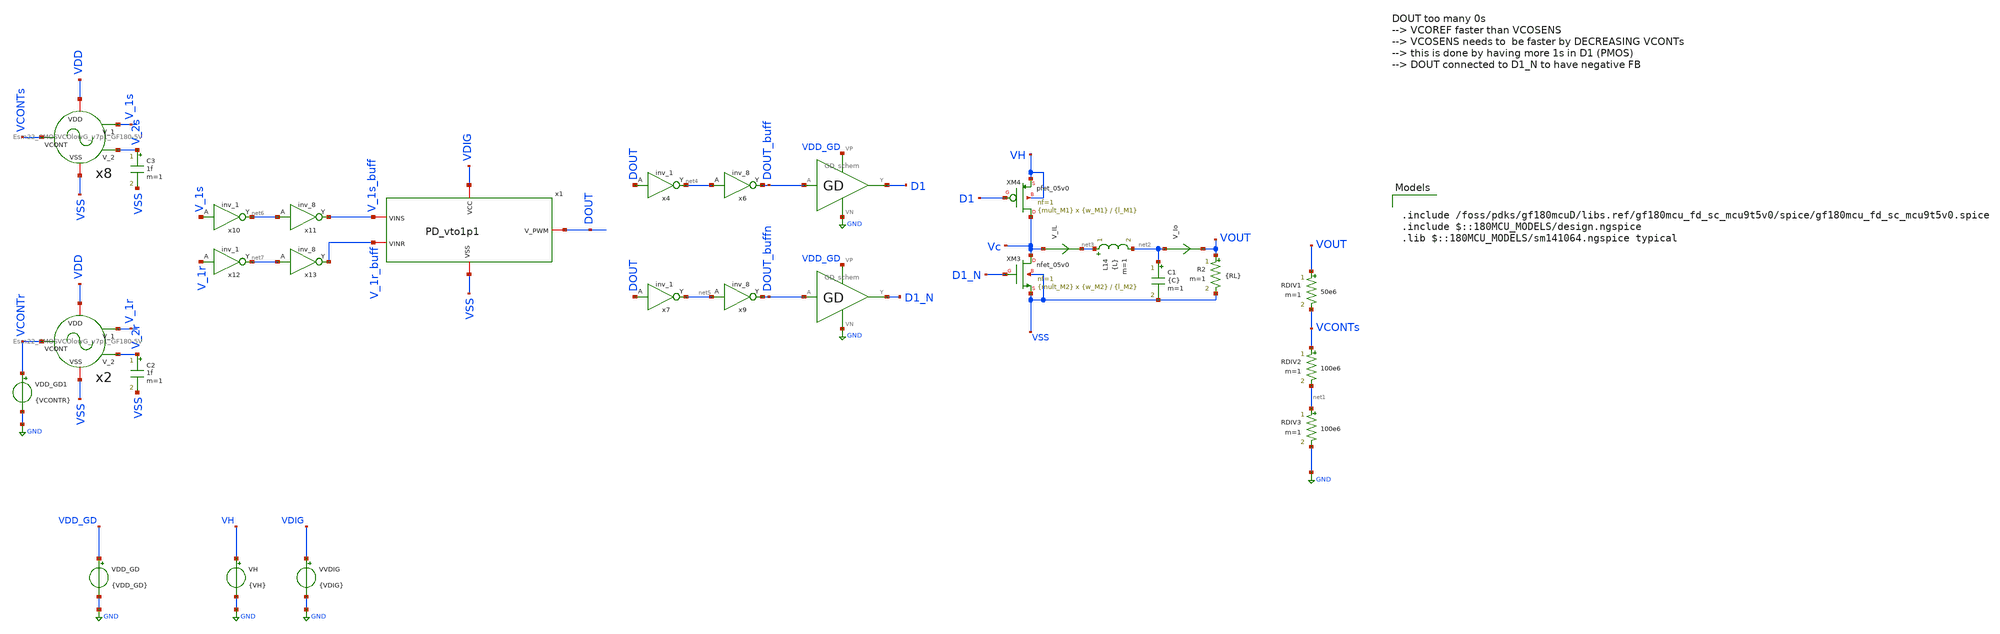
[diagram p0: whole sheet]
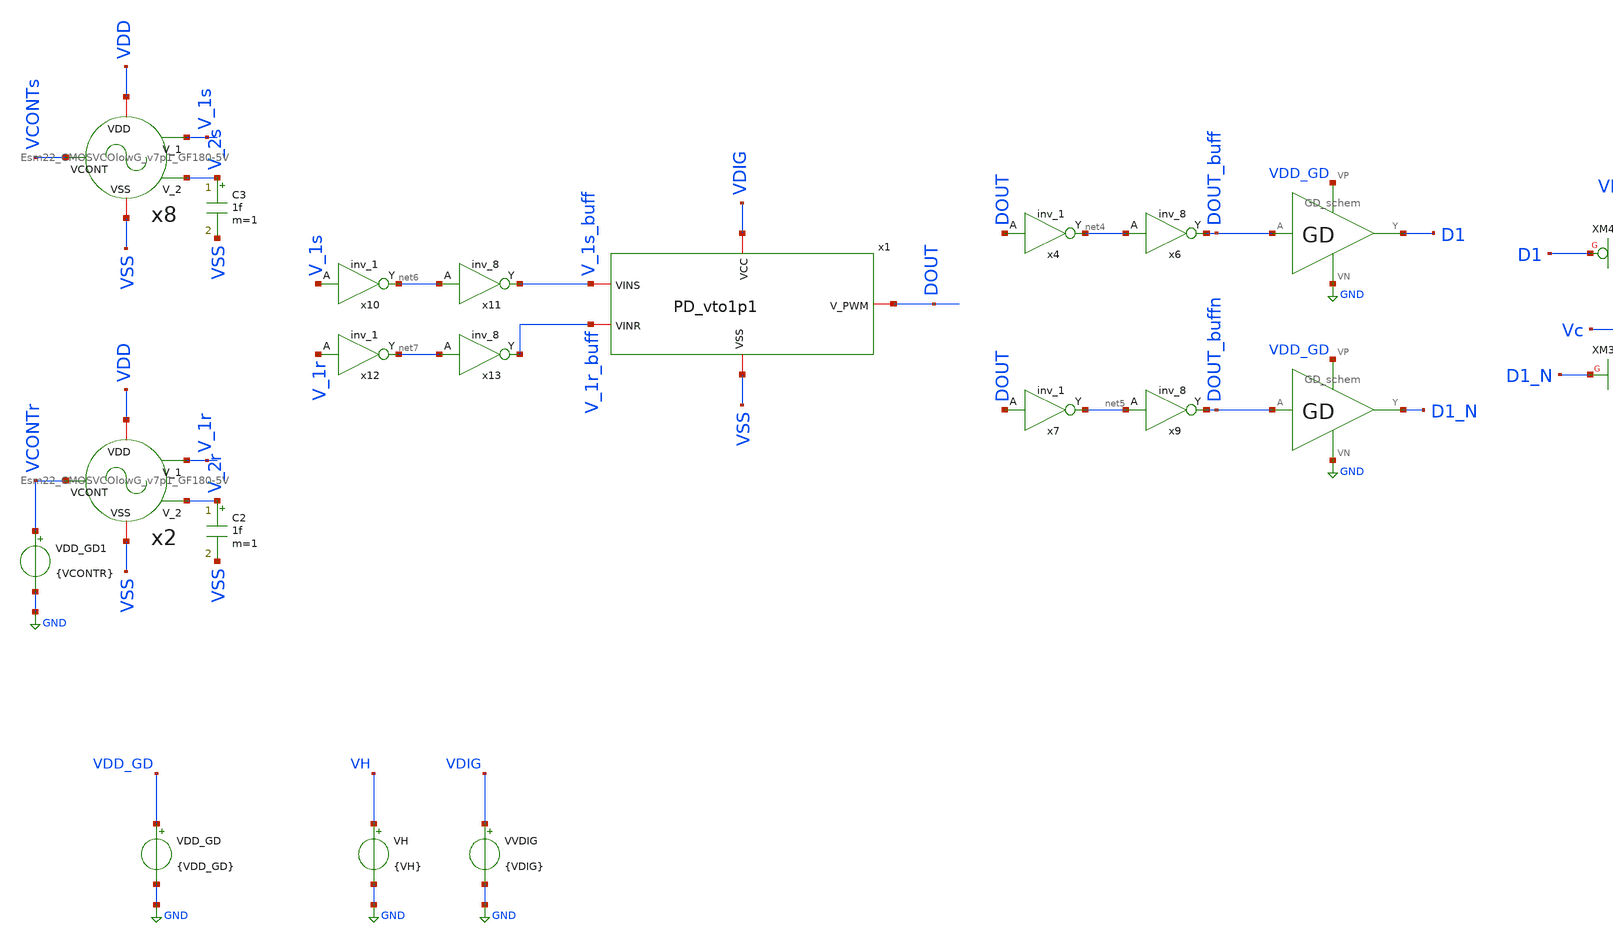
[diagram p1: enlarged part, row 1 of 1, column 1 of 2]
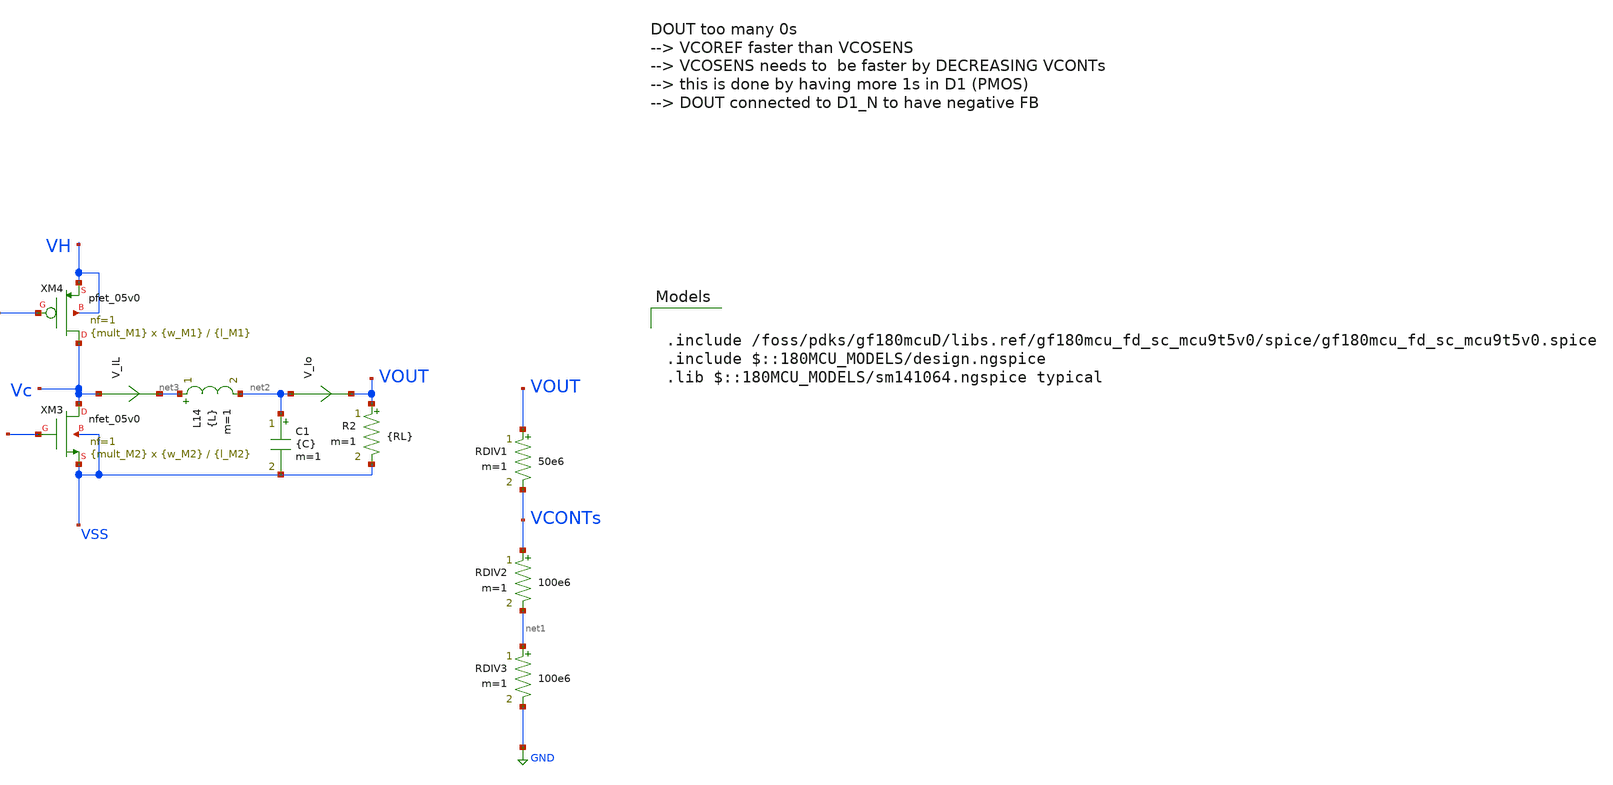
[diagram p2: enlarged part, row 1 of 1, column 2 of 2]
** sch_path: xschem/top/tb_TDBuckTOP-IHP-CL_v7p1.sch
**.subckt tb_TDBuckTOP-IHP-CL_v7p1
VH VH GND {VH}
VVDIG VDIG GND {VDIG}
RDIV1 VOUT VCONTs 50e6 m=1
RDIV2 VCONTs net1 100e6 m=1
RDIV3 net1 GND 100e6 m=1
VDD_GD VDD_GD GND {VDD_GD}
L14 net3 net2 {L} m=1
C1 net2 VSS {C} m=1
V_Io net2 VOUT 0
.save i(v_io)
V_IL Vc net3 0
.save i(v_il)
R2 VOUT VSS {RL} m=1
XM3 Vc D1_N VSS VSS nfet_05v0 L={l_M2} W={w_M2} nf=1 ad='int((nf+1)/2) * W/nf * 0.18u' as='int((nf+2)/2) * W/nf * 0.18u'
+ pd='2*int((nf+1)/2) * (W/nf + 0.18u)' ps='2*int((nf+2)/2) * (W/nf + 0.18u)' nrd='0.18u / W' nrs='0.18u / W'
+ sa=0 sb=0 sd=0 m={mult_M2}
XM4 Vc D1 VH VH pfet_05v0 L={l_M1} W={w_M1} nf=1 ad='int((nf+1)/2) * W/nf * 0.18u' as='int((nf+2)/2) * W/nf * 0.18u'
+ pd='2*int((nf+1)/2) * (W/nf + 0.18u)' ps='2*int((nf+2)/2) * (W/nf + 0.18u)' nrd='0.18u / W' nrs='0.18u / W'
+ sa=0 sb=0 sd=0 m={mult_M1}
x1 VDIG VSS V_1s_buff DOUT V_1r_buff PD_vto1p1
x8 VCONTs VSS VDD V_1s V_2s Esm22_CMOSVCOlowG_v7p1_GF180-5V
x2 VCONTr VSS VDD V_1r V_2r Esm22_CMOSVCOlowG_v7p1_GF180-5V
C2 V_2r VSS 1f m=1
C3 V_2s VSS 1f m=1
X3 VDD_GD GND DOUT_buff D1 GD_schem
X5 VDD_GD GND DOUT_buffn D1_N GD_schem
x4 DOUT VSS VDIG VSS VDIG net4 gf180mcu_fd_sc_mcu9t5v0__inv_1
x6 net4 VSS VDIG VSS VDIG DOUT_buff gf180mcu_fd_sc_mcu9t5v0__inv_8
x7 DOUT VSS VDIG VSS VDIG net5 gf180mcu_fd_sc_mcu9t5v0__inv_1
x9 net5 VSS VDIG VSS VDIG DOUT_buffn gf180mcu_fd_sc_mcu9t5v0__inv_8
VDD_GD1 VCONTr GND {VCONTR}
x10 V_1s VSS VDIG VSS VDIG net6 gf180mcu_fd_sc_mcu9t5v0__inv_1
x11 net6 VSS VDIG VSS VDIG V_1s_buff gf180mcu_fd_sc_mcu9t5v0__inv_8
x12 V_1r VSS VDIG VSS VDIG net7 gf180mcu_fd_sc_mcu9t5v0__inv_1
x13 net7 VSS VDIG VSS VDIG V_1r_buff gf180mcu_fd_sc_mcu9t5v0__inv_8
**** begin user architecture code

.param VDIG = 5
.param VH = 5
.param VDD_GD = 5
.param VCONTR = 2.64
*LATEST TDBuckLOADS
*300mA
.param RL = 6
*270mA
*.param RL = 6.67
*240mA
*.param RL = 7.5
*210mA
*.param RL = 8.57
*180mA
*.param RL = 10
*150mA
*.param RL = 12
*120mA
*.param RL = 15
*60mA
*.param RL = 30
*30mA
*.param RL = 60
*15mA
*.param RL = 120
.save v(VOUT) v(D1) v(D1_N) v(DOUT) v(VCONTr) v(VCONTs) v(V_1r) v(V_1s) v(DOUT_buff) v(DOUT_buffn) v(vh) i(vh) v(vdd_gd) i(vdd_gd) i(v_res) v(VCONTs_OL) v(vcp) v(vcn) i(vldo_out) i(vvdig) i(vvdd)
*.save all
vvdd vdd 0 dc 5
vvss vss 0 0
*vvconts VCONTs 0 dc 0.61
*.option temp = 200
.ic v(VCONTs) = 2
.ic v(V_1s) = 2
.ic v(V_2s) = 4
.ic v(V_1r) = 5
.ic v(V_2r) = 0
.ic v(VOUT) = 2.5

.control
*tran 2n 1m
*tran 4n 250u
tran 100p 30u
*wrdata /foss/designs/TO202406_CMOSVCO_Esm22/xschem/data/dataVSENS_2xCMOSVCOnDFF_v1p1.txt v(V_1s)
*+ tran1.v(V_1s) tran2.v(V_1s) tran3.v(V_1s) tran4.v(V_1s) tran5.v(V_1s) tran6.v(V_1s) tran7.v(V_1s) tran8.v(V_1s)
*+ tran9.v(V_1s) tran10.v(V_1s) tran11.v(V_1s) tran12.v(V_1s) tran13.v(V_1s) tran14.v(V_1s) tran15.v(V_1s)
*+ tran16.v(V_1s) tran17.v(V_1s) tran18.v(V_1s) tran19.v(V_1s)
*wrdata /foss/designs/TO202406_CMOSVCO_Esm22/xschem/data/data_TDBuckTOP-CL_v5p3_RL60.txt tran.v(vh)
*+ tran.i(vh) tran.v(VOUT) tran.i(vldo_out) tran.v(vh_gd) tran.i(vh_gd) tran.i(vvdig) tran.i(vvdd)
plot v(VOUT)
plot v(v_res)
plot v(D1) v(D1_N)+5
plot v(DOUT)
plot v(V_1s)+5 v(V_1r)+10
plot v(VCONTr) v(VCONTs)
*plot v(VCONTs_OL)
.endc





*PMOS
.param mult_gd_p = 72
.param w_gd_p = 6.4u
.param l_gd_p = 0.5u
*NMOS
.param mult_gd_n = 72
.param w_gd_n = 2u
.param l_gd_n = 0.6u





.param temp=27
.param mult_M1 = 2000
.param w_M1 =10u
.param l_M1 = 0.5u


.param mult_M2 = 625
.param w_M2 =10u
.param l_M2 =0.6u

*PMOS
.param mult_gd_p = 72
.param w_gd_p = 6.4u
.param l_gd_p = 0.5u
*NMOS
.param mult_gd_n = 72
.param w_gd_n = 2u
.param l_gd_n = 0.6u






*.param L = 550n
*.param R = 16.7
*.param C = 640n
.param L = 220n
*.param L = 440n
*.param C = 1u
.param C = 150n
*.param C = 300n




.include /foss/pdks/gf180mcuD/libs.ref/gf180mcu_fd_sc_mcu9t5v0/spice/gf180mcu_fd_sc_mcu9t5v0.spice
.include $::180MCU_MODELS/design.ngspice
.lib $::180MCU_MODELS/sm141064.ngspice typical

**** end user architecture code
**.ends

* expanding   symbol:  gf180_digital/PD/PD_vto1p1.sym # of pins=5
** sym_path: xschem/gf180_digital/PD/PD_vto1p1.sym
** sch_path: xschem/gf180_digital/PD/PD_vto1p1.sch
.subckt PD_vto1p1 VCC VSS VINS V_PWM VINR
*.iopin V_PWM
*.iopin VCC
*.iopin VSS
*.iopin VINS
*.iopin VINR
C2 VFE1 VSS 100f m=1
C1 VFE1 VSS 100f m=1
x1 V_N net1 VSS VCC VSS VCC V_PWM gf180mcu_fd_sc_mcu9t5v0__nor2_1
x3 VCC VSS VFE1 VINR net2 SPG_vto1p1
x2 VCC VSS VFE1 VINS net1 SPG_vto1p1
x4 net2 V_PWM VSS VCC VSS VCC V_N gf180mcu_fd_sc_mcu9t5v0__nor2_1
.ends


* expanding   symbol:  vco/Esm22_CMOSVCOlowG_v7p1_GF180-5V.sym # of pins=5
** sym_path: xschem/vco/Esm22_CMOSVCOlowG_v7p1_GF180-5V.sym
** sch_path: xschem/vco/Esm22_CMOSVCOlowG_v7p1_GF180-5V.sch
.subckt Esm22_CMOSVCOlowG_v7p1_GF180-5V VCONT VSS VDD V_1 V_2
*.ipin VCONT
*.iopin VDD
*.iopin VSS
*.opin V_1
*.opin V_2
x1 VDD VCONT V_1 V_5 VSS stage_v7p1_GF180-5V
x2 VDD VCONT V_2 V_1 VSS stage_v7p1_GF180-5V
x3 VDD VCONT V_3 V_2 VSS stage_v7p1_GF180-5V
x4 VDD VCONT V_4 V_3 VSS stage_v7p1_GF180-5V
x5 VDD VCONT V_5 V_4 VSS stage_v7p1_GF180-5V
.ends


* expanding   symbol:  pwr_stage/GD_schem.sym # of pins=4
** sym_path: pwr_stage/GD_schem.sym
** sch_path: pwr_stage/GD_schem.sch
.subckt GD_schem VP VN A Y
*.ipin A
*.iopin VP
*.iopin VN
*.opin Y
XM11 Y net1 VN VN nfet_05v0 L={l_gd_n} W={w_gd_n} nf=1 ad='int((nf+1)/2) * W/nf * 0.18u' as='int((nf+2)/2) * W/nf * 0.18u'
+ pd='2*int((nf+1)/2) * (W/nf + 0.18u)' ps='2*int((nf+2)/2) * (W/nf + 0.18u)' nrd='0.18u / W' nrs='0.18u / W'
+ sa=0 sb=0 sd=0 m={mult_gd_n}
XM12 Y net1 VP VP pfet_05v0 L={l_gd_p} W={w_gd_p} nf=1 ad='int((nf+1)/2) * W/nf * 0.18u' as='int((nf+2)/2) * W/nf * 0.18u'
+ pd='2*int((nf+1)/2) * (W/nf + 0.18u)' ps='2*int((nf+2)/2) * (W/nf + 0.18u)' nrd='0.18u / W' nrs='0.18u / W'
+ sa=0 sb=0 sd=0 m={mult_gd_p}
XM13 net1 A VN VN nfet_05v0 L={l_gd_n} W={w_gd_n} nf=1 ad='int((nf+1)/2) * W/nf * 0.18u' as='int((nf+2)/2) * W/nf * 0.18u'
+ pd='2*int((nf+1)/2) * (W/nf + 0.18u)' ps='2*int((nf+2)/2) * (W/nf + 0.18u)' nrd='0.18u / W' nrs='0.18u / W'
+ sa=0 sb=0 sd=0 m={mult_gd_n}/4
XM14 net1 A VP VP pfet_05v0 L={l_gd_p} W={w_gd_p} nf=1 ad='int((nf+1)/2) * W/nf * 0.18u' as='int((nf+2)/2) * W/nf * 0.18u'
+ pd='2*int((nf+1)/2) * (W/nf + 0.18u)' ps='2*int((nf+2)/2) * (W/nf + 0.18u)' nrd='0.18u / W' nrs='0.18u / W'
+ sa=0 sb=0 sd=0 m={mult_gd_p}/4
.ends


* expanding   symbol:  gf180_digital/SPG/SPG_vto1p1.sym # of pins=5
** sym_path: xschem/gf180_digital/SPG/SPG_vto1p1.sym
** sch_path: xschem/gf180_digital/SPG/SPG_vto1p1.sch
.subckt SPG_vto1p1 VDDd VSSd VFE VIN VRE
*.iopin VIN
*.iopin VFE
*.iopin VRE
*.iopin VDDd
*.iopin VSSd
x2 predly VSSd VDDd VSSd VDDd net2 gf180mcu_fd_sc_mcu9t5v0__inv_1
x3 vinn VSSd VDDd VSSd VDDd predly gf180mcu_fd_sc_mcu9t5v0__inv_1
x4 dly8 VSSd VDDd VSSd VDDd net1 gf180mcu_fd_sc_mcu9t5v0__inv_1
x5 VIN VSSd VDDd VSSd VDDd vinn gf180mcu_fd_sc_mcu9t5v0__inv_2
x6 predly VSSd VDDd VSSd VDDd V_gatein gf180mcu_fd_sc_mcu9t5v0__inv_8
x9 VDDd VSSd V_gatein dly7 large_delay_vto1p1
x1 dly7 VSSd VDDd VSSd VDDd dly8 gf180mcu_fd_sc_mcu9t5v0__inv_8
x8 net2 dly8 VFE VDDd VDDd VSSd VSSd gf180mcu_fd_sc_mcu9t5v0__and2_1
x7 net1 predly VRE VDDd VDDd VSSd VSSd gf180mcu_fd_sc_mcu9t5v0__and2_1
.ends


* expanding   symbol:  vco/stage_v7p1_GF180-5V.sym # of pins=5
** sym_path: xschem/vco/stage_v7p1_GF180-5V.sym
** sch_path: xschem/vco/stage_v7p1_GF180-5V.sch
.subckt stage_v7p1_GF180-5V VDD VCONT VOUT VIN VSS
*.ipin VIN
*.opin VOUT
*.iopin VDD
*.iopin VSS
*.ipin VCONT
XMN1 net4 net4 VSS VSS nfet_05v0 L=0.70u W=7u nf=7 ad='int((nf+1)/2) * W/nf * 0.18u' as='int((nf+2)/2) * W/nf * 0.18u'
+ pd='2*int((nf+1)/2) * (W/nf + 0.18u)' ps='2*int((nf+2)/2) * (W/nf + 0.18u)' nrd='0.18u / W' nrs='0.18u / W'
+ sa=0 sb=0 sd=0 m=1
XMN2 net3 net4 VSS VSS nfet_05v0 L=0.70u W=7u nf=7 ad='int((nf+1)/2) * W/nf * 0.18u' as='int((nf+2)/2) * W/nf * 0.18u'
+ pd='2*int((nf+1)/2) * (W/nf + 0.18u)' ps='2*int((nf+2)/2) * (W/nf + 0.18u)' nrd='0.18u / W' nrs='0.18u / W'
+ sa=0 sb=0 sd=0 m=1
XMN3 net2 net4 VSS VSS nfet_05v0 L=0.70u W=4u nf=4 ad='int((nf+1)/2) * W/nf * 0.18u' as='int((nf+2)/2) * W/nf * 0.18u'
+ pd='2*int((nf+1)/2) * (W/nf + 0.18u)' ps='2*int((nf+2)/2) * (W/nf + 0.18u)' nrd='0.18u / W' nrs='0.18u / W'
+ sa=0 sb=0 sd=0 m=1
XMN4 VOUT VIN net2 VSS nfet_05v0 L=5u W=2u nf=1 ad='int((nf+1)/2) * W/nf * 0.18u' as='int((nf+2)/2) * W/nf * 0.18u'
+ pd='2*int((nf+1)/2) * (W/nf + 0.18u)' ps='2*int((nf+2)/2) * (W/nf + 0.18u)' nrd='0.18u / W' nrs='0.18u / W'
+ sa=0 sb=0 sd=0 m=1
XMP2 net3 net3 VDD VDD pfet_05v0 L=4u W=8u nf=8 ad='int((nf+1)/2) * W/nf * 0.18u' as='int((nf+2)/2) * W/nf * 0.18u'
+ pd='2*int((nf+1)/2) * (W/nf + 0.18u)' ps='2*int((nf+2)/2) * (W/nf + 0.18u)' nrd='0.18u / W' nrs='0.18u / W'
+ sa=0 sb=0 sd=0 m=1
XMP3 net1 net3 VDD VDD pfet_05v0 L=4u W=5u nf=5 ad='int((nf+1)/2) * W/nf * 0.18u' as='int((nf+2)/2) * W/nf * 0.18u'
+ pd='2*int((nf+1)/2) * (W/nf + 0.18u)' ps='2*int((nf+2)/2) * (W/nf + 0.18u)' nrd='0.18u / W' nrs='0.18u / W'
+ sa=0 sb=0 sd=0 m=1
XMP1 net4 VCONT VDD VDD pfet_05v0 L=7u W=0.5u nf=1 ad='int((nf+1)/2) * W/nf * 0.18u' as='int((nf+2)/2) * W/nf * 0.18u'
+ pd='2*int((nf+1)/2) * (W/nf + 0.18u)' ps='2*int((nf+2)/2) * (W/nf + 0.18u)' nrd='0.18u / W' nrs='0.18u / W'
+ sa=0 sb=0 sd=0 m=1
XMP4 VOUT VIN net1 VDD pfet_05v0 L=5u W=5u nf=1 ad='int((nf+1)/2) * W/nf * 0.18u' as='int((nf+2)/2) * W/nf * 0.18u'
+ pd='2*int((nf+1)/2) * (W/nf + 0.18u)' ps='2*int((nf+2)/2) * (W/nf + 0.18u)' nrd='0.18u / W' nrs='0.18u / W'
+ sa=0 sb=0 sd=0 m=1
XMP5 net4 VSS VDD VDD pfet_05v0 L=7u W=0.5u nf=1 ad='int((nf+1)/2) * W/nf * 0.18u' as='int((nf+2)/2) * W/nf * 0.18u'
+ pd='2*int((nf+1)/2) * (W/nf + 0.18u)' ps='2*int((nf+2)/2) * (W/nf + 0.18u)' nrd='0.18u / W' nrs='0.18u / W'
+ sa=0 sb=0 sd=0 m=1
.ends


* expanding   symbol:  gf180_digital/large_delay/large_delay_vto1p1.sym # of pins=4
** sym_path: xschem/gf180_digital/large_delay/large_delay_vto1p1.sym
** sch_path: xschem/gf180_digital/large_delay/large_delay_vto1p1.sch
.subckt large_delay_vto1p1 VDDd VSSd VIN VOUT
*.iopin VIN
*.iopin VOUT
*.iopin VDDd
*.iopin VSSd
x1 VIN VOUT VDDd VDDd VSSd VSSd gf180mcu_fd_sc_mcu9t5v0__dlya_1
.ends

.GLOBAL GND
.end
